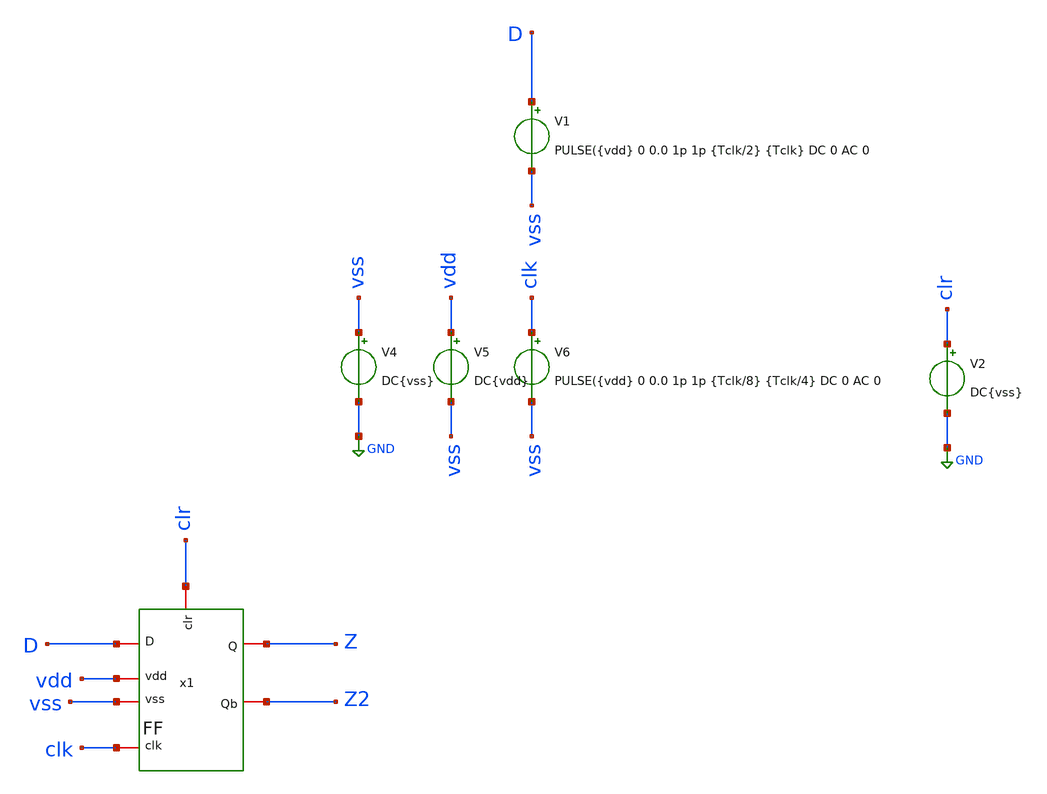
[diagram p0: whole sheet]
** sch_path: tstbnch/ff_test.sch
**.subckt ff_test
V4 vss GND DC{vss}
V5 vdd vss DC{vdd}
V6 clk vss PULSE({vdd} 0 0.0 1p 1p {Tclk/8} {Tclk/4} DC 0 AC 0
V1 D vss PULSE({vdd} 0 0.0 1p 1p {Tclk/2} {Tclk} DC 0 AC 0
V2 clr GND DC{vss}
x1 D Z Z2 vss vdd clk clr FF
**** begin user architecture code


* Circuit Parameters
.param vdd = 1.8
.param vss = 0.0
.param Tclk = 20n
.options TEMP = 65.0
* Include Models
.lib /foss/pdks/sky130A/libs.tech/ngspice/sky130.lib.spice TT
* OP Parameters & Singals to save
.save all



*Simulations

.control

tran 0.01u 100n
setplot tran1
plot v(clk) v(D)+2 v(Z)+4 v(Z2)+6
reset

set filetype = ascii
write dcsweep.raw
.endc
.end


**** end user architecture code
**.ends

* expanding   symbol:  /foss/designs/sch/FF.sym # of pins=7
** sym_path: sch/FF.sym
** sch_path: sch/FF.sch
.subckt FF D Q Qb vss vdd clk clr
*.iopin clk
*.iopin clr
*.iopin vdd
*.iopin vss
*.iopin D
*.iopin Q
*.iopin Qb
x1 clk vdd vss D net1 n_clk TG
x3 n_clk vdd vss net2 net3 clk TG
x5 clk vdd vss Qb net3 n_clk TG
x9 n_clk vdd vss net4 net1 clk TG
x2 vss vdd net3 clr Q NOR
x6 vss vdd clr net2 net4 NOR
x4 vdd net1 net2 vss inverter
x7 vdd clk n_clk vss inverter
x8 vdd Q Qb vss inverter
.ends


* expanding   symbol:  /foss/designs/sch/TG.sym # of pins=6
** sym_path: sch/TG.sym
** sch_path: sch/TG.sch
.subckt TG clk vdd vss IN OUT n_clk
*.iopin OUT
*.iopin IN
*.iopin clk
*.iopin n_clk
*.iopin vdd
*.iopin vss
XM1 OUT clk IN vss sky130_fd_pr__nfet_01v8 L=0.15 W=0.75 nf=1 ad='int((nf+1)/2) * W/nf * 0.29' as='int((nf+2)/2) * W/nf * 0.29'
+ pd='2*int((nf+1)/2) * (W/nf + 0.29)' ps='2*int((nf+2)/2) * (W/nf + 0.29)' nrd='0.29 / W' nrs='0.29 / W'
+ sa=0 sb=0 sd=0 mult=1 m=1
XM2 OUT n_clk IN vdd sky130_fd_pr__pfet_01v8 L=0.15 W=1.5 nf=1 ad='int((nf+1)/2) * W/nf * 0.29' as='int((nf+2)/2) * W/nf * 0.29'
+ pd='2*int((nf+1)/2) * (W/nf + 0.29)' ps='2*int((nf+2)/2) * (W/nf + 0.29)' nrd='0.29 / W' nrs='0.29 / W'
+ sa=0 sb=0 sd=0 mult=1 m=1
.ends


* expanding   symbol:  /foss/designs/sch/NOR.sym # of pins=5
** sym_path: sch/NOR.sym
** sch_path: sch/NOR.sch
.subckt NOR vss vdd A B vout
*.iopin A
*.iopin vdd
*.iopin vss
*.iopin vout
*.iopin B
XM8 vout A vss vss sky130_fd_pr__nfet_01v8 L=0.15 W=0.75 nf=1 ad='int((1 + 1)/2) * 0.75 / 1 * 0.29' as='int((1 + 2)/2) * 0.75 / 1 * 0.29'
+ pd='2*int((1 + 1)/2) * (0.75 / 1 + 0.29)' ps='2*int((1 + 2)/2) * (0.75 / 1 + 0.29)' nrd='0.29 / 0.75 '
+ nrs='0.29 / 0.75 ' sa=0 sb=0 sd=0 mult=1 m=1
XM9 vout B vss vss sky130_fd_pr__nfet_01v8 L=0.15 W=0.75 nf=1 ad='int((1 + 1)/2) * 0.75 / 1 * 0.29' as='int((1 + 2)/2) * 0.75 / 1 * 0.29'
+ pd='2*int((1 + 1)/2) * (0.75 / 1 + 0.29)' ps='2*int((1 + 2)/2) * (0.75 / 1 + 0.29)' nrd='0.29 / 0.75 '
+ nrs='0.29 / 0.75 ' sa=0 sb=0 sd=0 mult=1 m=1
XM7 vout A net1 vdd sky130_fd_pr__pfet_01v8 L=0.15 W=3 nf=1 ad='int((nf+1)/2) * W/nf * 0.29' as='int((nf+2)/2) * W/nf * 0.29'
+ pd='2*int((nf+1)/2) * (W/nf + 0.29)' ps='2*int((nf+2)/2) * (W/nf + 0.29)' nrd='0.29 / W' nrs='0.29 / W'
+ sa=0 sb=0 sd=0 mult=1 m=1
XM6 net1 B vdd vdd sky130_fd_pr__pfet_01v8 L=0.15 W=3 nf=1 ad='int((nf+1)/2) * W/nf * 0.29' as='int((nf+2)/2) * W/nf * 0.29'
+ pd='2*int((nf+1)/2) * (W/nf + 0.29)' ps='2*int((nf+2)/2) * (W/nf + 0.29)' nrd='0.29 / W' nrs='0.29 / W'
+ sa=0 sb=0 sd=0 mult=1 m=1
.ends


* expanding   symbol:  /foss/designs/sch/inverter.sym # of pins=4
** sym_path: sch/inverter.sym
** sch_path: sch/inverter.sch
.subckt inverter vdd in out vss
*.iopin out
*.iopin vdd
*.iopin vss
*.iopin in
XM1 out in vss vss sky130_fd_pr__nfet_01v8 L=0.15 W=0.45 nf=1 ad='int((nf+1)/2) * W/nf * 0.29' as='int((nf+2)/2) * W/nf * 0.29'
+ pd='2*int((nf+1)/2) * (W/nf + 0.29)' ps='2*int((nf+2)/2) * (W/nf + 0.29)' nrd='0.29 / W' nrs='0.29 / W'
+ sa=0 sb=0 sd=0 mult=1 m=1
XM2 out in vdd vdd sky130_fd_pr__pfet_01v8 L=0.15 W=0.45 nf=1 ad='int((nf+1)/2) * W/nf * 0.29' as='int((nf+2)/2) * W/nf * 0.29'
+ pd='2*int((nf+1)/2) * (W/nf + 0.29)' ps='2*int((nf+2)/2) * (W/nf + 0.29)' nrd='0.29 / W' nrs='0.29 / W'
+ sa=0 sb=0 sd=0 mult=1 m=1
.ends

.GLOBAL GND
.end
